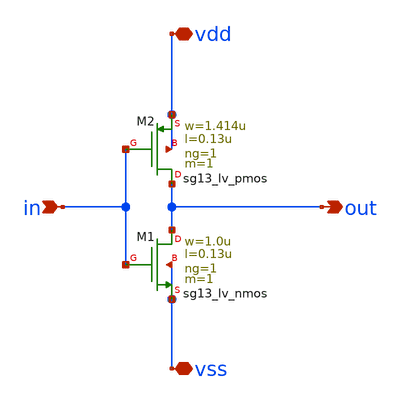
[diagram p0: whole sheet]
** sch_path: designs/p1-pbit/characterisation/xschem/ihp_sg13g2_inv.sch
**.subckt ihp_sg13g2_inv in out vdd vss
*.ipin in
*.opin out
*.iopin vdd
*.iopin vss
XM2 out in vdd vdd sg13_lv_pmos w=1.414u l=0.13u ng=1 m=1 mm_ok=1
XM1 out in vss vss sg13_lv_nmos w=1.0u l=0.13u ng=1 m=1 mm_ok=1
**.ends
.end
